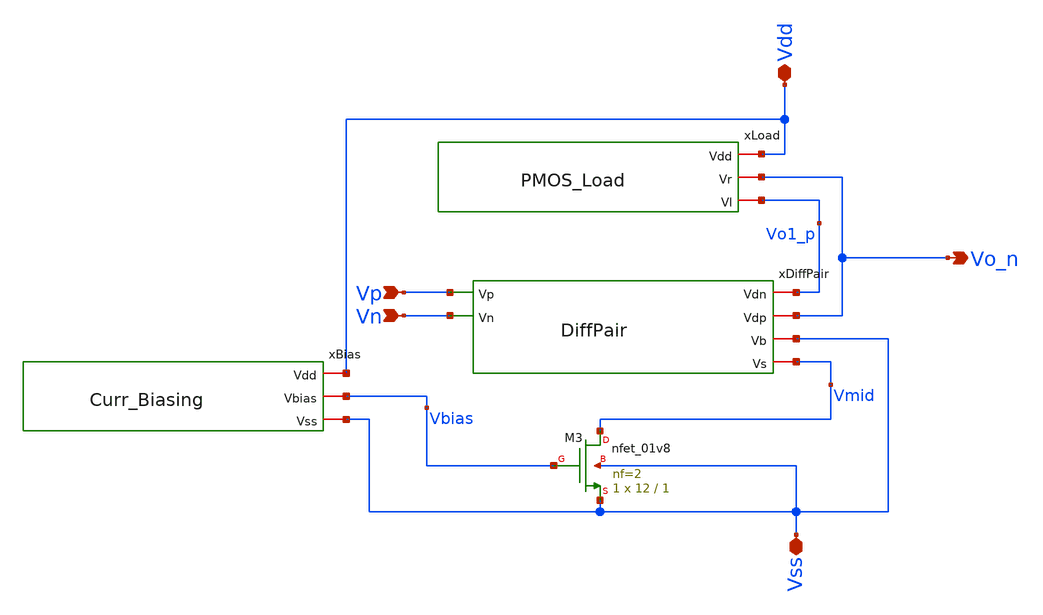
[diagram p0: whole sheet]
** sch_path: Circuits/DiffAmp/DiffAmp.sch
**.subckt DiffAmp Vp Vn Vdd Vss Vo_n
*.ipin Vp
*.ipin Vn
*.iopin Vdd
*.iopin Vss
*.opin Vo_n
xDiffPair Vo1_p Vo_n Vss Vp Vn Vmid DiffPair
xBias Vdd Vbias Vss Curr_Biasing
xLoad Vdd Vo_n Vo1_p PMOS_Load
XM3 Vmid Vbias Vss Vss sky130_fd_pr__nfet_01v8 L=1 W=12 nf=2 ad='int((nf+1)/2) * W/nf * 0.29' as='int((nf+2)/2) * W/nf * 0.29'
+ pd='2*int((nf+1)/2) * (W/nf + 0.29)' ps='2*int((nf+2)/2) * (W/nf + 0.29)' nrd='0.29 / W' nrs='0.29 / W'
+ sa=0 sb=0 sd=0 mult=1 m=1
**.ends
.end
